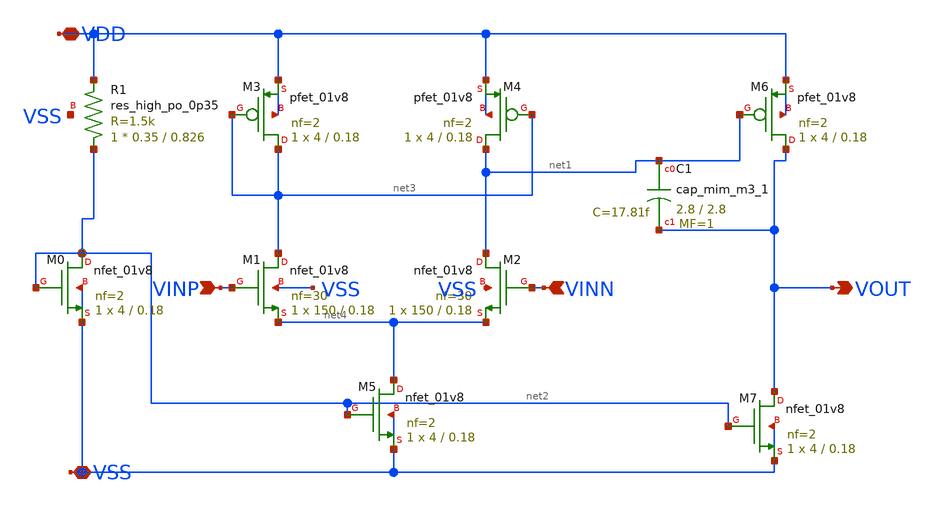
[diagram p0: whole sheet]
** sch_path: schematic/opamp.sch
**.subckt opamp VINN VINP VSS VDD VOUT
*.ipin VINN
*.ipin VINP
*.iopin VSS
*.iopin VDD
*.opin VOUT
XM0 net2 net2 VSS VSS sky130_fd_pr__nfet_01v8 L=0.18 W=4 nf=2 ad='int((2 + 1)/2) * 4 / 2 * 0.29' as='int((2 + 2)/2) * 4 / 2 * 0.29'
+ pd='2*int((2 + 1)/2) * (4 / 2 + 0.29)' ps='2*int((2 + 2)/2) * (4 / 2 + 0.29)' nrd='0.29 / 4 ' nrs='0.29 / 4 '
+ sa=0 sb=0 sd=0 mult=1 m=1
XR1 net2 VDD VSS sky130_fd_pr__res_high_po_0p35 L=0.826 mult=1 m=1
XM1 net3 VINP net4 VSS sky130_fd_pr__nfet_01v8 L=0.18 W=150 nf=30 ad='int((30 + 1)/2) * 150 / 30 * 0.29'
+ as='int((30 + 2)/2) * 150 / 30 * 0.29' pd='2*int((30 + 1)/2) * (150 / 30 + 0.29)' ps='2*int((30 + 2)/2) * (150 / 30 + 0.29)'
+ nrd='0.29 / 150 ' nrs='0.29 / 150 ' sa=0 sb=0 sd=0 mult=1 m=1
XM2 net1 VINN net4 VSS sky130_fd_pr__nfet_01v8 L=0.18 W=150 nf=30 ad='int((30 + 1)/2) * 150 / 30 * 0.29'
+ as='int((30 + 2)/2) * 150 / 30 * 0.29' pd='2*int((30 + 1)/2) * (150 / 30 + 0.29)' ps='2*int((30 + 2)/2) * (150 / 30 + 0.29)'
+ nrd='0.29 / 150 ' nrs='0.29 / 150 ' sa=0 sb=0 sd=0 mult=1 m=1
XM3 net3 net3 VDD VDD sky130_fd_pr__pfet_01v8 L=0.18 W=4 nf=2 ad='int((2 + 1)/2) * 4 / 2 * 0.29' as='int((2 + 2)/2) * 4 / 2 * 0.29'
+ pd='2*int((2 + 1)/2) * (4 / 2 + 0.29)' ps='2*int((2 + 2)/2) * (4 / 2 + 0.29)' nrd='0.29 / 4 ' nrs='0.29 / 4 '
+ sa=0 sb=0 sd=0 mult=1 m=1
XM4 net1 net3 VDD VDD sky130_fd_pr__pfet_01v8 L=0.18 W=4 nf=2 ad='int((2 + 1)/2) * 4 / 2 * 0.29' as='int((2 + 2)/2) * 4 / 2 * 0.29'
+ pd='2*int((2 + 1)/2) * (4 / 2 + 0.29)' ps='2*int((2 + 2)/2) * (4 / 2 + 0.29)' nrd='0.29 / 4 ' nrs='0.29 / 4 '
+ sa=0 sb=0 sd=0 mult=1 m=1
XM5 net4 net2 VSS VSS sky130_fd_pr__nfet_01v8 L=0.18 W=4 nf=2 ad='int((2 + 1)/2) * 4 / 2 * 0.29' as='int((2 + 2)/2) * 4 / 2 * 0.29'
+ pd='2*int((2 + 1)/2) * (4 / 2 + 0.29)' ps='2*int((2 + 2)/2) * (4 / 2 + 0.29)' nrd='0.29 / 4 ' nrs='0.29 / 4 '
+ sa=0 sb=0 sd=0 mult=1 m=1
XM6 VOUT net1 VDD VDD sky130_fd_pr__pfet_01v8 L=0.18 W=4 nf=2 ad='int((2 + 1)/2) * 4 / 2 * 0.29' as='int((2 + 2)/2) * 4 / 2 * 0.29'
+ pd='2*int((2 + 1)/2) * (4 / 2 + 0.29)' ps='2*int((2 + 2)/2) * (4 / 2 + 0.29)' nrd='0.29 / 4 ' nrs='0.29 / 4 '
+ sa=0 sb=0 sd=0 mult=1 m=1
XM7 VOUT net2 VSS VSS sky130_fd_pr__nfet_01v8 L=0.18 W=4 nf=2 ad='int((2 + 1)/2) * 4 / 2 * 0.29' as='int((2 + 2)/2) * 4 / 2 * 0.29'
+ pd='2*int((2 + 1)/2) * (4 / 2 + 0.29)' ps='2*int((2 + 2)/2) * (4 / 2 + 0.29)' nrd='0.29 / 4 ' nrs='0.29 / 4 '
+ sa=0 sb=0 sd=0 mult=1 m=1
XC1 net1 VOUT sky130_fd_pr__cap_mim_m3_1 W=2.8 L=2.8 MF=1 m=1
**.ends
.end
